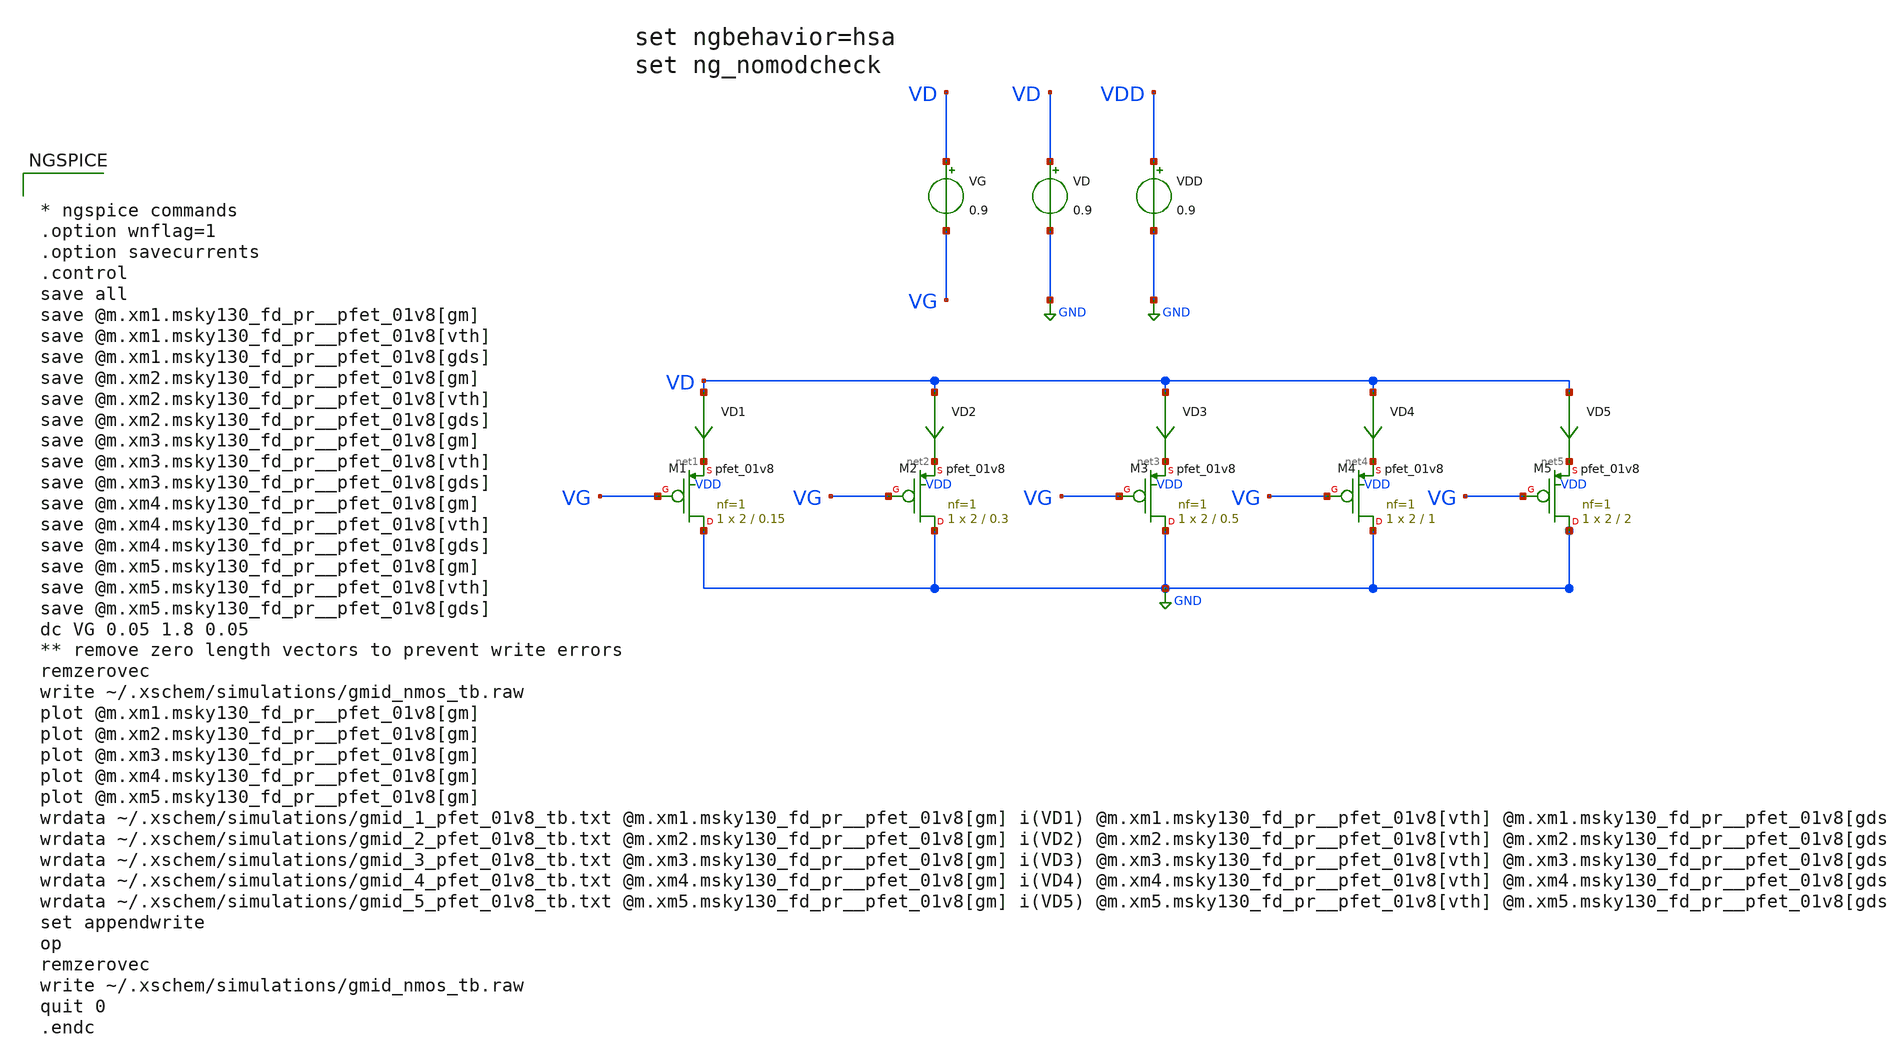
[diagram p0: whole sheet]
** sch_path: designs/gmid_pmos_1v8_tb.sch
**.subckt gmid_pmos_1v8_tb
VG VD VG 0.9
VD VD GND 0.9
VD1 VD net1 0
.save i(vd1)
VD2 VD net2 0
.save i(vd2)
XM1 GND VG net1 VDD sky130_fd_pr__pfet_01v8 L=0.15 W=2 nf=1 ad='int((nf+1)/2) * W/nf * 0.29' as='int((nf+2)/2) * W/nf * 0.29'
+ pd='2*int((nf+1)/2) * (W/nf + 0.29)' ps='2*int((nf+2)/2) * (W/nf + 0.29)' nrd='0.29 / W' nrs='0.29 / W'
+ sa=0 sb=0 sd=0 mult=1 m=1
XM2 GND VG net2 VDD sky130_fd_pr__pfet_01v8 L=0.3 W=2 nf=1 ad='int((nf+1)/2) * W/nf * 0.29' as='int((nf+2)/2) * W/nf * 0.29'
+ pd='2*int((nf+1)/2) * (W/nf + 0.29)' ps='2*int((nf+2)/2) * (W/nf + 0.29)' nrd='0.29 / W' nrs='0.29 / W'
+ sa=0 sb=0 sd=0 mult=1 m=1
VD3 VD net3 0
.save i(vd3)
XM3 GND VG net3 VDD sky130_fd_pr__pfet_01v8 L=0.5 W=2 nf=1 ad='int((nf+1)/2) * W/nf * 0.29' as='int((nf+2)/2) * W/nf * 0.29'
+ pd='2*int((nf+1)/2) * (W/nf + 0.29)' ps='2*int((nf+2)/2) * (W/nf + 0.29)' nrd='0.29 / W' nrs='0.29 / W'
+ sa=0 sb=0 sd=0 mult=1 m=1
VD4 VD net4 0
.save i(vd4)
XM4 GND VG net4 VDD sky130_fd_pr__pfet_01v8 L=1 W=2 nf=1 ad='int((nf+1)/2) * W/nf * 0.29' as='int((nf+2)/2) * W/nf * 0.29'
+ pd='2*int((nf+1)/2) * (W/nf + 0.29)' ps='2*int((nf+2)/2) * (W/nf + 0.29)' nrd='0.29 / W' nrs='0.29 / W'
+ sa=0 sb=0 sd=0 mult=1 m=1
VD5 VD net5 0
.save i(vd5)
XM5 GND VG net5 VDD sky130_fd_pr__pfet_01v8 L=2 W=2 nf=1 ad='int((nf+1)/2) * W/nf * 0.29' as='int((nf+2)/2) * W/nf * 0.29'
+ pd='2*int((nf+1)/2) * (W/nf + 0.29)' ps='2*int((nf+2)/2) * (W/nf + 0.29)' nrd='0.29 / W' nrs='0.29 / W'
+ sa=0 sb=0 sd=0 mult=1 m=1
VDD VDD GND 0.9
**** begin user architecture code

** opencircuitdesign pdks install
.lib $::SKYWATER_MODELS/sky130.lib.spice ff




* ngspice commands
.option wnflag=1
.option savecurrents
.control
save all
save @m.xm1.msky130_fd_pr__pfet_01v8[gm]
save @m.xm1.msky130_fd_pr__pfet_01v8[vth]
save @m.xm1.msky130_fd_pr__pfet_01v8[gds]
save @m.xm2.msky130_fd_pr__pfet_01v8[gm]
save @m.xm2.msky130_fd_pr__pfet_01v8[vth]
save @m.xm2.msky130_fd_pr__pfet_01v8[gds]
save @m.xm3.msky130_fd_pr__pfet_01v8[gm]
save @m.xm3.msky130_fd_pr__pfet_01v8[vth]
save @m.xm3.msky130_fd_pr__pfet_01v8[gds]
save @m.xm4.msky130_fd_pr__pfet_01v8[gm]
save @m.xm4.msky130_fd_pr__pfet_01v8[vth]
save @m.xm4.msky130_fd_pr__pfet_01v8[gds]
save @m.xm5.msky130_fd_pr__pfet_01v8[gm]
save @m.xm5.msky130_fd_pr__pfet_01v8[vth]
save @m.xm5.msky130_fd_pr__pfet_01v8[gds]
dc VG 0.05 1.8 0.05
** remove zero length vectors to prevent write errors
remzerovec
write ~/.xschem/simulations/gmid_nmos_tb.raw
plot @m.xm1.msky130_fd_pr__pfet_01v8[gm]
plot @m.xm2.msky130_fd_pr__pfet_01v8[gm]
plot @m.xm3.msky130_fd_pr__pfet_01v8[gm]
plot @m.xm4.msky130_fd_pr__pfet_01v8[gm]
plot @m.xm5.msky130_fd_pr__pfet_01v8[gm]
wrdata ~/.xschem/simulations/gmid_1_pfet_01v8_tb.txt @m.xm1.msky130_fd_pr__pfet_01v8[gm] i(VD1)
+ @m.xm1.msky130_fd_pr__pfet_01v8[vth] @m.xm1.msky130_fd_pr__pfet_01v8[gds]
wrdata ~/.xschem/simulations/gmid_2_pfet_01v8_tb.txt @m.xm2.msky130_fd_pr__pfet_01v8[gm] i(VD2)
+ @m.xm2.msky130_fd_pr__pfet_01v8[vth] @m.xm2.msky130_fd_pr__pfet_01v8[gds]
wrdata ~/.xschem/simulations/gmid_3_pfet_01v8_tb.txt @m.xm3.msky130_fd_pr__pfet_01v8[gm] i(VD3)
+ @m.xm3.msky130_fd_pr__pfet_01v8[vth] @m.xm3.msky130_fd_pr__pfet_01v8[gds]
wrdata ~/.xschem/simulations/gmid_4_pfet_01v8_tb.txt @m.xm4.msky130_fd_pr__pfet_01v8[gm] i(VD4)
+ @m.xm4.msky130_fd_pr__pfet_01v8[vth] @m.xm4.msky130_fd_pr__pfet_01v8[gds]
wrdata ~/.xschem/simulations/gmid_5_pfet_01v8_tb.txt @m.xm5.msky130_fd_pr__pfet_01v8[gm] i(VD5)
+ @m.xm5.msky130_fd_pr__pfet_01v8[vth] @m.xm5.msky130_fd_pr__pfet_01v8[gds]
set appendwrite
op
remzerovec
write ~/.xschem/simulations/gmid_nmos_tb.raw
quit 0
.endc


**** end user architecture code
**.ends
.GLOBAL GND
.end
